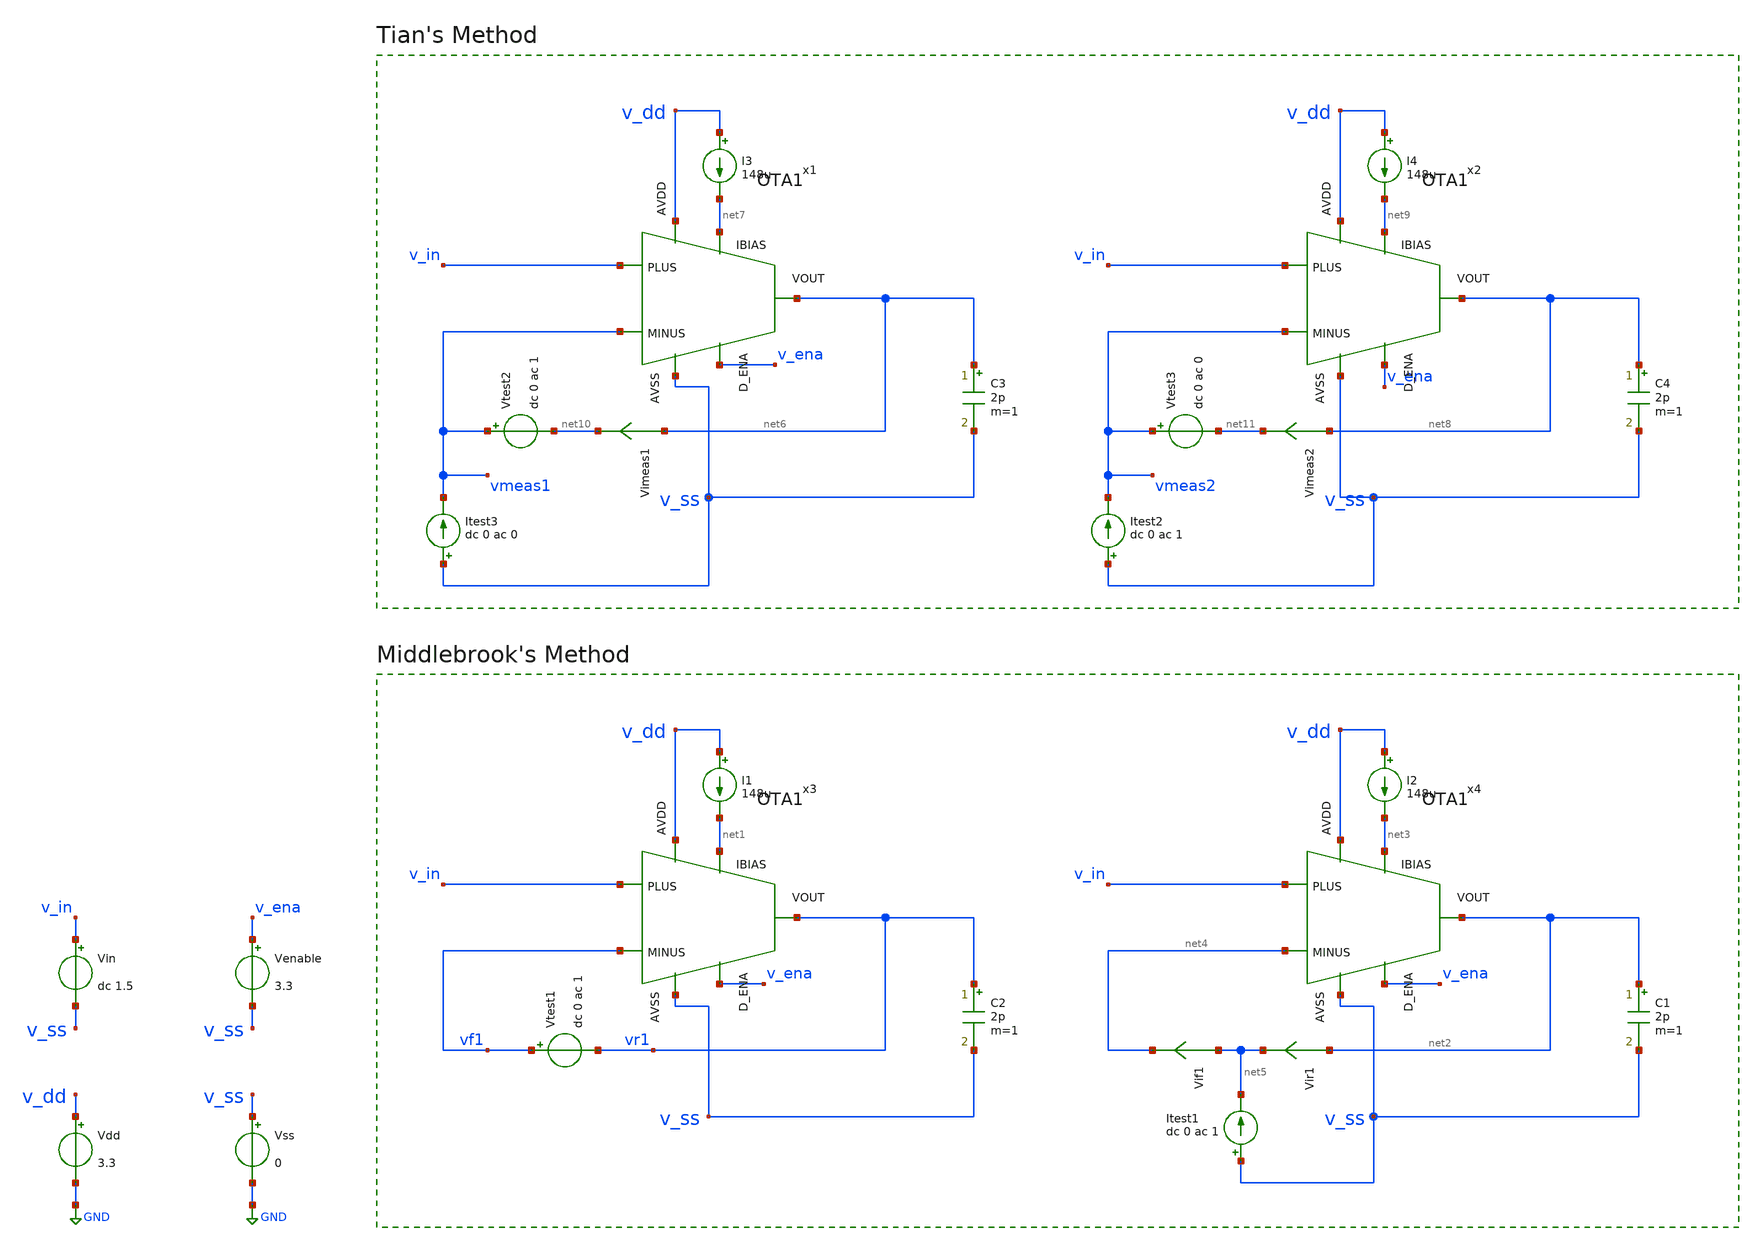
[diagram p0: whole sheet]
** sch_path: DSM_2ndOrder/1_Schematics/real_circuits/tb_ota1_loopgain.sch
* (c) 2024 H. Pretl, S. Dorrer, Apache-2.0 license
* DSM_2ndOrder/1_Schematics/real_circuits/3v3/OTA1.sch:
* (c) 2025 Thesis_HP, Apache-2.0 license
**.subckt tb_ota1_loopgain
Vdd v_dd GND 3.3
Vss v_ss GND 0
Vin v_in v_ss dc 1.5
Venable v_ena v_ss 3.3
C2 vr1 v_ss 2p m=1
I1 v_dd net1 148u
Vtest1 vf1 vr1 dc 0 ac 1
C1 net2 v_ss 2p m=1
I2 v_dd net3 148u
Vir1 net2 net5 0
.save i(vir1)
Vif1 net5 net4 0
.save i(vif1)
Itest1 v_ss net5 dc 0 ac 1
C3 net6 v_ss 2p m=1
I3 v_dd net7 148u
C4 net8 v_ss 2p m=1
I4 v_dd net9 148u
Itest3 v_ss vmeas1 dc 0 ac 0
Vtest2 vmeas1 net10 dc 0 ac 1
Vimeas1 net6 net10 0
.save i(vimeas1)
Itest2 v_ss vmeas2 dc 0 ac 1
Vtest3 vmeas2 net11 dc 0 ac 0
Vimeas2 net8 net11 0
.save i(vimeas2)
x1 v_dd net7 net6 vmeas1 v_in v_ena v_ss OTA1
x2 v_dd net9 net8 vmeas2 v_in v_ena v_ss OTA1
x3 v_dd net1 vr1 vf1 v_in v_ena v_ss OTA1
x4 v_dd net3 net2 net4 v_in v_ena v_ss OTA1
**** begin user architecture code

.lib cornerMOShv.lib mos_tt
.lib cornerRES.lib res_typ



.param temp=27
.options savecurrents reltol=1e-3 abstol=1e-12 gmin=1e-15
.control
save all

* Operating Point Analysis
op
remzerovec
write ota-improved_tb-loopgain.raw
set appendwrite

* AC Analysis
ac dec 101 1 100G
remzerovec
write ota-improved_tb-loopgain.raw
set appendwrite

* Middlebrook's Method
let tv=-v(vr1)/v(vf1)
let ti=-i(vir1)/i(vif1)
let tmb=(tv*ti - 1)/(tv + ti + 2)

plot db(tmb) ylabel 'Magnitude - Middlebrook'
plot 180/pi*cphase(tmb) ylabel 'Phase - Middlebrook'

* Tian's Method
* vtest=0, itest=1:
let A=i(Vimeas2)
let C=v(vmeas2)

* vtest=1, itest=0:
let B=i(Vimeas1)
let D=v(vmeas1)
let ttian=(A*D-B*C-A)/(2*(B*C-A*D)+A-D+1)

plot db(ttian) ylabel 'Magnitude - Tian'
plot 180/pi*cphase(ttian) ylabel 'Phase - Tian'

* Middlebrook vs. Tian
plot db(tmb) db(ttian) ylabel 'Magnitude'
plot 180/pi*cphase(tmb) 180/pi*cphase(ttian) ylabel 'Phase'

write ota-improved_tb-loopgain.raw

*quit
.endc


**** end user architecture code
**.ends

* expanding   symbol:  OTA1.sym # of pins=7
** sym_path: DSM_2ndOrder/1_Schematics/real_circuits/3v3/OTA1.sym
** sch_path: DSM_2ndOrder/1_Schematics/real_circuits/3v3/OTA1.sch
.subckt OTA1 AVDD IBIAS VOUT MINUS PLUS D_ENA AVSS
*.ipin AVSS
*.ipin IBIAS
*.ipin AVDD
*.ipin PLUS
*.ipin MINUS
*.opin VOUT
*.ipin D_ENA
XM23 IBIAS net3 AVSS AVSS sg13_hv_nmos w=13.8u l=1u ng=2 m=1 mm_ok=1
XM25 IBIAS net2 net3 AVSS sg13_hv_nmos w=1u l=0.5u ng=1 m=1 mm_ok=1
XM24 net10 net3 AVSS AVSS sg13_hv_nmos w=13.8u l=1u ng=2 m=1 mm_ok=1
XM19 net10 net5 net4 AVDD sg13_hv_pmos w=42.5u l=1u ng=10 m=1 mm_ok=1
XM20 net4 net4 AVDD AVDD sg13_hv_pmos w=42.5u l=1u ng=10 m=1 mm_ok=1
XM21 AVSS net5 net8 AVDD sg13_hv_pmos w=100u l=0.5u ng=10 m=1 mm_ok=1
XM22 net8 net4 AVDD AVDD sg13_hv_pmos w=42.5u l=1u ng=10 m=1 mm_ok=1
XM26 net7 net4 AVDD AVDD sg13_hv_pmos w=85.5u l=1u ng=10 m=1 mm_ok=1
XM27 net5 net8 net7 AVDD sg13_hv_pmos w=42.5u l=1u ng=10 m=1 mm_ok=1
XM28 net5 net15 net6 AVSS sg13_hv_nmos w=12u l=1u ng=2 m=1 mm_ok=1
XM29 net6 net5 AVSS AVSS sg13_hv_nmos w=12.5u l=1u ng=2 m=1 mm_ok=1
XM30 net9 net3 AVSS AVSS sg13_hv_nmos w=14u l=1u ng=2 m=1 mm_ok=1
XM31 net7 PLUS net9 AVSS sg13_hv_nmos w=14.5u l=0.8u ng=2 m=1 mm_ok=1
XM32 net11 MINUS net9 AVSS sg13_hv_nmos w=14.5u l=0.8u ng=2 m=1 mm_ok=1
XM42 AVDD net4 AVDD AVDD sg13_hv_pmos w=12u l=0.5u ng=4 m=1 mm_ok=1
XM41 AVDD net8 AVDD AVDD sg13_hv_pmos w=12u l=0.5u ng=4 m=1 mm_ok=1
XM38 AVSS net3 AVSS AVSS sg13_hv_nmos w=8u l=1u ng=4 m=1 mm_ok=1
XM33 net1 D_ENA AVDD AVDD sg13_hv_pmos w=1u l=0.5u ng=1 m=1 mm_ok=1
XM34 net2 net1 AVDD AVDD sg13_hv_pmos w=1u l=0.5u ng=1 m=1 mm_ok=1
XM35 net1 D_ENA AVSS AVSS sg13_hv_nmos w=1u l=0.5u ng=1 m=1 mm_ok=1
XM36 net2 net1 AVSS AVSS sg13_hv_nmos w=1u l=0.5u ng=1 m=1 mm_ok=1
XM37 net11 AVSS AVSS AVSS sg13_hv_nmos w=14.5u l=0.8u ng=2 m=1 mm_ok=1
XM39 VOUT net8 net11 AVDD sg13_hv_pmos w=42.5u l=1u ng=10 m=1 mm_ok=1
XM40 net11 net4 AVDD AVDD sg13_hv_pmos w=85.5u l=1u ng=10 m=1 mm_ok=1
XM43 VOUT net15 net12 AVSS sg13_hv_nmos w=12u l=1u ng=2 m=1 mm_ok=1
XM44 net12 net5 AVSS AVSS sg13_hv_nmos w=12.5u l=1u ng=2 m=1 mm_ok=1
XM45 net12 AVSS AVSS AVSS sg13_hv_nmos w=12.5u l=1u ng=2 m=1 mm_ok=1
XM46 VOUT AVSS AVSS AVSS sg13_hv_nmos w=12u l=1u ng=2 m=1 mm_ok=1
XM47 net11 AVDD AVDD AVDD sg13_hv_pmos w=85.5u l=1u ng=10 m=1 mm_ok=1
XM48 VOUT AVDD AVDD AVDD sg13_hv_pmos w=42.5u l=1u ng=10 m=1 mm_ok=1
XM49 net13 net4 AVDD AVDD sg13_hv_pmos w=85.5u l=1u ng=10 m=1 mm_ok=1
XM50 net13 VOUT net14 AVSS sg13_hv_nmos w=12u l=1u ng=2 m=1 mm_ok=1
XM51 net14 net14 AVSS AVSS sg13_hv_nmos w=12u l=1u ng=2 m=1 mm_ok=1
XM52 net15 net14 AVSS AVSS sg13_hv_nmos w=12u l=1u ng=2 m=1 mm_ok=1
XM53 AVDD VOUT net15 AVSS sg13_hv_nmos w=100u l=0.5u ng=10 m=1 mm_ok=1
XM54 AVSS net15 AVSS AVSS sg13_hv_nmos w=8u l=1u ng=4 m=1 mm_ok=1
XM55 net5 net1 AVSS AVSS sg13_hv_nmos w=1u l=0.5u ng=1 m=1 mm_ok=1
XM56 net7 AVSS AVSS AVSS sg13_hv_nmos w=14.5u l=0.8u ng=2 m=1 mm_ok=1
XM57 net5 AVDD AVDD AVDD sg13_hv_pmos w=42.5u l=1u ng=10 m=1 mm_ok=1
XM58 net6 AVSS AVSS AVSS sg13_hv_nmos w=12.5u l=1u ng=2 m=1 mm_ok=1
XM59 net5 AVSS AVSS AVSS sg13_hv_nmos w=12u l=1u ng=2 m=1 mm_ok=1
XM60 net4 AVDD AVDD AVDD sg13_hv_pmos w=42.5u l=1u ng=10 m=1 mm_ok=1
XM61 net14 AVSS AVSS AVSS sg13_hv_nmos w=12u l=1u ng=2 m=1 mm_ok=1
.ends

.GLOBAL GND
.end
